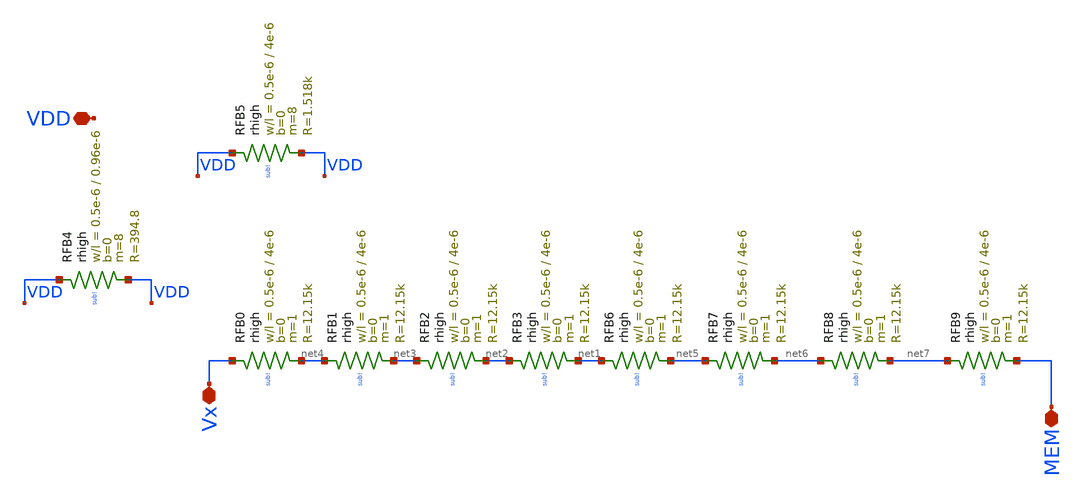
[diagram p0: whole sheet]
** sch_path: work/resistance_bench/resistence_bench.sch
**.subckt resistence_bench VDD Vx MEM
*.iopin VDD
*.iopin Vx
*.iopin MEM
XRFB0 Vx net4 sub! rhigh w=0.5e-6 l=4e-6 m=1 b=0 mm_ok=1
XRFB1 net4 net3 sub! rhigh w=0.5e-6 l=4e-6 m=1 b=0 mm_ok=1
XRFB2 net3 net2 sub! rhigh w=0.5e-6 l=4e-6 m=1 b=0 mm_ok=1
XRFB3 net2 net1 sub! rhigh w=0.5e-6 l=4e-6 m=1 b=0 mm_ok=1
XRFB5 VDD VDD sub! rhigh w=0.5e-6 l=4e-6 m=8 b=0 mm_ok=1
XRFB6 net1 net5 sub! rhigh w=0.5e-6 l=4e-6 m=1 b=0 mm_ok=1
XRFB7 net5 net6 sub! rhigh w=0.5e-6 l=4e-6 m=1 b=0 mm_ok=1
XRFB8 net6 net7 sub! rhigh w=0.5e-6 l=4e-6 m=1 b=0 mm_ok=1
XRFB9 net7 MEM sub! rhigh w=0.5e-6 l=4e-6 m=1 b=0 mm_ok=1
XRFB4 VDD VDD sub! rhigh w=0.5e-6 l=0.96e-6 m=8 b=0 mm_ok=1
**.ends
.end
